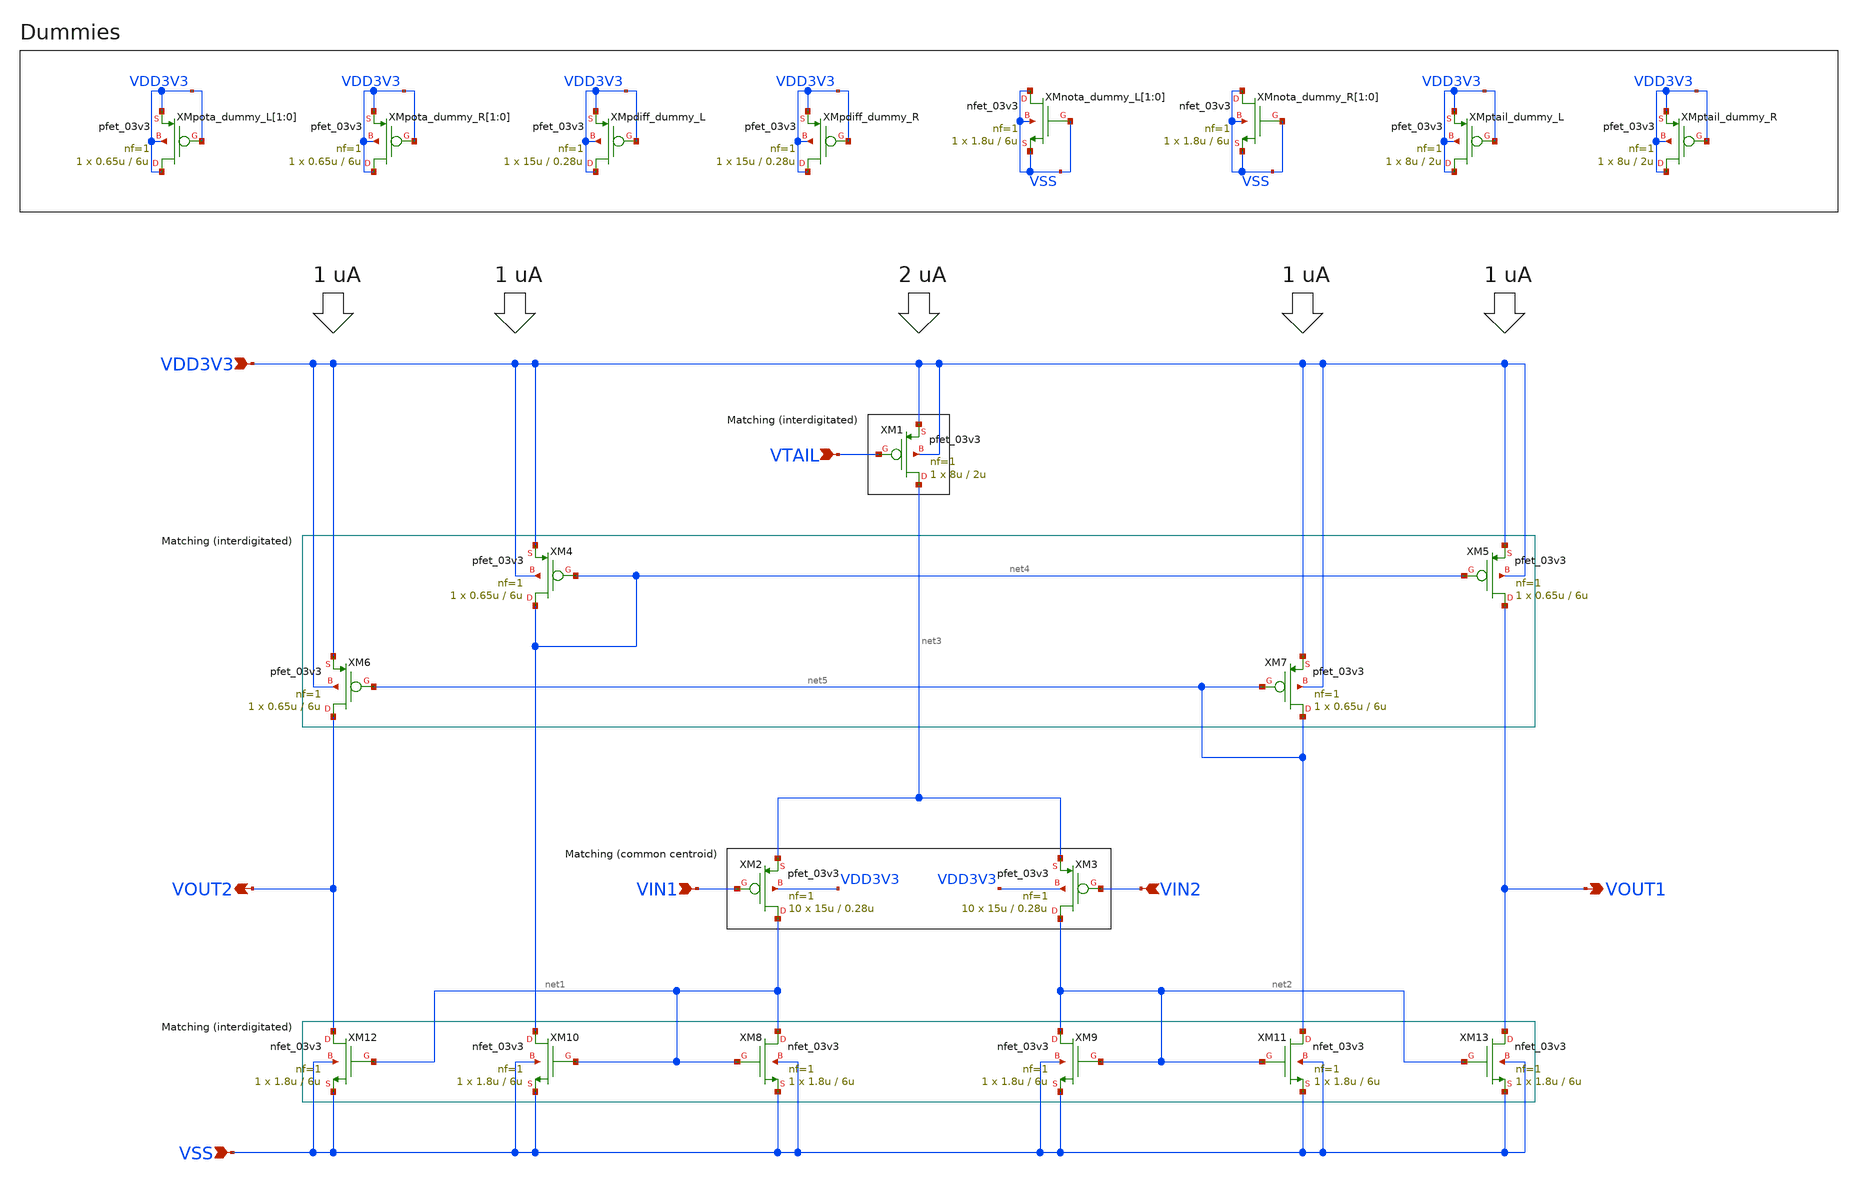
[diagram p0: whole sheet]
** sch_path: designs/libs/core_ina/ina_ota/ina_ota.sch
**.subckt ina_ota VIN1 VIN2 VTAIL VSS VOUT1 VDD3V3 VOUT2
*.ipin VIN1
*.ipin VIN2
*.ipin VTAIL
*.ipin VSS
*.opin VOUT1
*.ipin VDD3V3
*.opin VOUT2
XM4 net4 net4 VDD3V3 VDD3V3 pfet_03v3 L=6u W=0.65u nf=1 ad='int((nf+1)/2) * W/nf * 0.18u' as='int((nf+2)/2) * W/nf * 0.18u'
+ pd='2*int((nf+1)/2) * (W/nf + 0.18u)' ps='2*int((nf+2)/2) * (W/nf + 0.18u)' nrd='0.18u / W' nrs='0.18u / W'
+ sa=0 sb=0 sd=0 m=1
XM1 net3 VTAIL VDD3V3 VDD3V3 pfet_03v3 L=2u W=8u nf=1 ad='int((nf+1)/2) * W/nf * 0.18u' as='int((nf+2)/2) * W/nf * 0.18u'
+ pd='2*int((nf+1)/2) * (W/nf + 0.18u)' ps='2*int((nf+2)/2) * (W/nf + 0.18u)' nrd='0.18u / W' nrs='0.18u / W'
+ sa=0 sb=0 sd=0 m=1
XM7 net5 net5 VDD3V3 VDD3V3 pfet_03v3 L=6u W=0.65u nf=1 ad='int((nf+1)/2) * W/nf * 0.18u' as='int((nf+2)/2) * W/nf * 0.18u'
+ pd='2*int((nf+1)/2) * (W/nf + 0.18u)' ps='2*int((nf+2)/2) * (W/nf + 0.18u)' nrd='0.18u / W' nrs='0.18u / W'
+ sa=0 sb=0 sd=0 m=1
XM2 net1 VIN1 net3 VDD3V3 pfet_03v3 L=0.28u W=15u nf=1 ad='int((nf+1)/2) * W/nf * 0.18u' as='int((nf+2)/2) * W/nf * 0.18u'
+ pd='2*int((nf+1)/2) * (W/nf + 0.18u)' ps='2*int((nf+2)/2) * (W/nf + 0.18u)' nrd='0.18u / W' nrs='0.18u / W'
+ sa=0 sb=0 sd=0 m=10
XM3 net2 VIN2 net3 VDD3V3 pfet_03v3 L=0.28u W=15u nf=1 ad='int((nf+1)/2) * W/nf * 0.18u' as='int((nf+2)/2) * W/nf * 0.18u'
+ pd='2*int((nf+1)/2) * (W/nf + 0.18u)' ps='2*int((nf+2)/2) * (W/nf + 0.18u)' nrd='0.18u / W' nrs='0.18u / W'
+ sa=0 sb=0 sd=0 m=10
XM10 net4 net1 VSS VSS nfet_03v3 L=6u W=1.8u nf=1 ad='int((nf+1)/2) * W/nf * 0.18u' as='int((nf+2)/2) * W/nf * 0.18u'
+ pd='2*int((nf+1)/2) * (W/nf + 0.18u)' ps='2*int((nf+2)/2) * (W/nf + 0.18u)' nrd='0.18u / W' nrs='0.18u / W'
+ sa=0 sb=0 sd=0 m=1
XM11 net5 net2 VSS VSS nfet_03v3 L=6u W=1.8u nf=1 ad='int((nf+1)/2) * W/nf * 0.18u' as='int((nf+2)/2) * W/nf * 0.18u'
+ pd='2*int((nf+1)/2) * (W/nf + 0.18u)' ps='2*int((nf+2)/2) * (W/nf + 0.18u)' nrd='0.18u / W' nrs='0.18u / W'
+ sa=0 sb=0 sd=0 m=1
XM8 net1 net1 VSS VSS nfet_03v3 L=6u W=1.8u nf=1 ad='int((nf+1)/2) * W/nf * 0.18u' as='int((nf+2)/2) * W/nf * 0.18u'
+ pd='2*int((nf+1)/2) * (W/nf + 0.18u)' ps='2*int((nf+2)/2) * (W/nf + 0.18u)' nrd='0.18u / W' nrs='0.18u / W'
+ sa=0 sb=0 sd=0 m=1
XM9 net2 net2 VSS VSS nfet_03v3 L=6u W=1.8u nf=1 ad='int((nf+1)/2) * W/nf * 0.18u' as='int((nf+2)/2) * W/nf * 0.18u'
+ pd='2*int((nf+1)/2) * (W/nf + 0.18u)' ps='2*int((nf+2)/2) * (W/nf + 0.18u)' nrd='0.18u / W' nrs='0.18u / W'
+ sa=0 sb=0 sd=0 m=1
XM5 VOUT1 net4 VDD3V3 VDD3V3 pfet_03v3 L=6u W=0.65u nf=1 ad='int((nf+1)/2) * W/nf * 0.18u' as='int((nf+2)/2) * W/nf * 0.18u'
+ pd='2*int((nf+1)/2) * (W/nf + 0.18u)' ps='2*int((nf+2)/2) * (W/nf + 0.18u)' nrd='0.18u / W' nrs='0.18u / W'
+ sa=0 sb=0 sd=0 m=1
XM13 VOUT1 net2 VSS VSS nfet_03v3 L=6u W=1.8u nf=1 ad='int((nf+1)/2) * W/nf * 0.18u' as='int((nf+2)/2) * W/nf * 0.18u'
+ pd='2*int((nf+1)/2) * (W/nf + 0.18u)' ps='2*int((nf+2)/2) * (W/nf + 0.18u)' nrd='0.18u / W' nrs='0.18u / W'
+ sa=0 sb=0 sd=0 m=1
XM12 VOUT2 net1 VSS VSS nfet_03v3 L=6u W=1.8u nf=1 ad='int((nf+1)/2) * W/nf * 0.18u' as='int((nf+2)/2) * W/nf * 0.18u'
+ pd='2*int((nf+1)/2) * (W/nf + 0.18u)' ps='2*int((nf+2)/2) * (W/nf + 0.18u)' nrd='0.18u / W' nrs='0.18u / W'
+ sa=0 sb=0 sd=0 m=1
XM6 VOUT2 net5 VDD3V3 VDD3V3 pfet_03v3 L=6u W=0.65u nf=1 ad='int((nf+1)/2) * W/nf * 0.18u' as='int((nf+2)/2) * W/nf * 0.18u'
+ pd='2*int((nf+1)/2) * (W/nf + 0.18u)' ps='2*int((nf+2)/2) * (W/nf + 0.18u)' nrd='0.18u / W' nrs='0.18u / W'
+ sa=0 sb=0 sd=0 m=1
XMpota_dummy_L[1] VDD3V3 VDD3V3 VDD3V3 VDD3V3 pfet_03v3 L=6u W=0.65u nf=1 ad='int((nf+1)/2) * W/nf * 0.18u'
+ as='int((nf+2)/2) * W/nf * 0.18u' pd='2*int((nf+1)/2) * (W/nf + 0.18u)' ps='2*int((nf+2)/2) * (W/nf + 0.18u)'
+ nrd='0.18u / W' nrs='0.18u / W' sa=0 sb=0 sd=0 m=1
XMpota_dummy_L[0] VDD3V3 VDD3V3 VDD3V3 VDD3V3 pfet_03v3 L=6u W=0.65u nf=1 ad='int((nf+1)/2) * W/nf * 0.18u'
+ as='int((nf+2)/2) * W/nf * 0.18u' pd='2*int((nf+1)/2) * (W/nf + 0.18u)' ps='2*int((nf+2)/2) * (W/nf + 0.18u)'
+ nrd='0.18u / W' nrs='0.18u / W' sa=0 sb=0 sd=0 m=1
XMpdiff_dummy_L VDD3V3 VDD3V3 VDD3V3 VDD3V3 pfet_03v3 L=0.28u W=15u nf=1 ad='int((nf+1)/2) * W/nf * 0.18u'
+ as='int((nf+2)/2) * W/nf * 0.18u' pd='2*int((nf+1)/2) * (W/nf + 0.18u)' ps='2*int((nf+2)/2) * (W/nf + 0.18u)'
+ nrd='0.18u / W' nrs='0.18u / W' sa=0 sb=0 sd=0 m=1
XMpota_dummy_R[1] VDD3V3 VDD3V3 VDD3V3 VDD3V3 pfet_03v3 L=6u W=0.65u nf=1 ad='int((nf+1)/2) * W/nf * 0.18u'
+ as='int((nf+2)/2) * W/nf * 0.18u' pd='2*int((nf+1)/2) * (W/nf + 0.18u)' ps='2*int((nf+2)/2) * (W/nf + 0.18u)'
+ nrd='0.18u / W' nrs='0.18u / W' sa=0 sb=0 sd=0 m=1
XMpota_dummy_R[0] VDD3V3 VDD3V3 VDD3V3 VDD3V3 pfet_03v3 L=6u W=0.65u nf=1 ad='int((nf+1)/2) * W/nf * 0.18u'
+ as='int((nf+2)/2) * W/nf * 0.18u' pd='2*int((nf+1)/2) * (W/nf + 0.18u)' ps='2*int((nf+2)/2) * (W/nf + 0.18u)'
+ nrd='0.18u / W' nrs='0.18u / W' sa=0 sb=0 sd=0 m=1
XMpdiff_dummy_R VDD3V3 VDD3V3 VDD3V3 VDD3V3 pfet_03v3 L=0.28u W=15u nf=1 ad='int((nf+1)/2) * W/nf * 0.18u'
+ as='int((nf+2)/2) * W/nf * 0.18u' pd='2*int((nf+1)/2) * (W/nf + 0.18u)' ps='2*int((nf+2)/2) * (W/nf + 0.18u)'
+ nrd='0.18u / W' nrs='0.18u / W' sa=0 sb=0 sd=0 m=1
XMnota_dummy_L[1] VSS VSS VSS VSS nfet_03v3 L=6u W=1.8u nf=1 ad='int((nf+1)/2) * W/nf * 0.18u' as='int((nf+2)/2) * W/nf * 0.18u'
+ pd='2*int((nf+1)/2) * (W/nf + 0.18u)' ps='2*int((nf+2)/2) * (W/nf + 0.18u)' nrd='0.18u / W' nrs='0.18u / W'
+ sa=0 sb=0 sd=0 m=1
XMnota_dummy_L[0] VSS VSS VSS VSS nfet_03v3 L=6u W=1.8u nf=1 ad='int((nf+1)/2) * W/nf * 0.18u' as='int((nf+2)/2) * W/nf * 0.18u'
+ pd='2*int((nf+1)/2) * (W/nf + 0.18u)' ps='2*int((nf+2)/2) * (W/nf + 0.18u)' nrd='0.18u / W' nrs='0.18u / W'
+ sa=0 sb=0 sd=0 m=1
XMnota_dummy_R[1] VSS VSS VSS VSS nfet_03v3 L=6u W=1.8u nf=1 ad='int((nf+1)/2) * W/nf * 0.18u' as='int((nf+2)/2) * W/nf * 0.18u'
+ pd='2*int((nf+1)/2) * (W/nf + 0.18u)' ps='2*int((nf+2)/2) * (W/nf + 0.18u)' nrd='0.18u / W' nrs='0.18u / W'
+ sa=0 sb=0 sd=0 m=1
XMnota_dummy_R[0] VSS VSS VSS VSS nfet_03v3 L=6u W=1.8u nf=1 ad='int((nf+1)/2) * W/nf * 0.18u' as='int((nf+2)/2) * W/nf * 0.18u'
+ pd='2*int((nf+1)/2) * (W/nf + 0.18u)' ps='2*int((nf+2)/2) * (W/nf + 0.18u)' nrd='0.18u / W' nrs='0.18u / W'
+ sa=0 sb=0 sd=0 m=1
XMptail_dummy_L VDD3V3 VDD3V3 VDD3V3 VDD3V3 pfet_03v3 L=2u W=8u nf=1 ad='int((nf+1)/2) * W/nf * 0.18u'
+ as='int((nf+2)/2) * W/nf * 0.18u' pd='2*int((nf+1)/2) * (W/nf + 0.18u)' ps='2*int((nf+2)/2) * (W/nf + 0.18u)'
+ nrd='0.18u / W' nrs='0.18u / W' sa=0 sb=0 sd=0 m=1
XMptail_dummy_R VDD3V3 VDD3V3 VDD3V3 VDD3V3 pfet_03v3 L=2u W=8u nf=1 ad='int((nf+1)/2) * W/nf * 0.18u'
+ as='int((nf+2)/2) * W/nf * 0.18u' pd='2*int((nf+1)/2) * (W/nf + 0.18u)' ps='2*int((nf+2)/2) * (W/nf + 0.18u)'
+ nrd='0.18u / W' nrs='0.18u / W' sa=0 sb=0 sd=0 m=1
**.ends
.end
